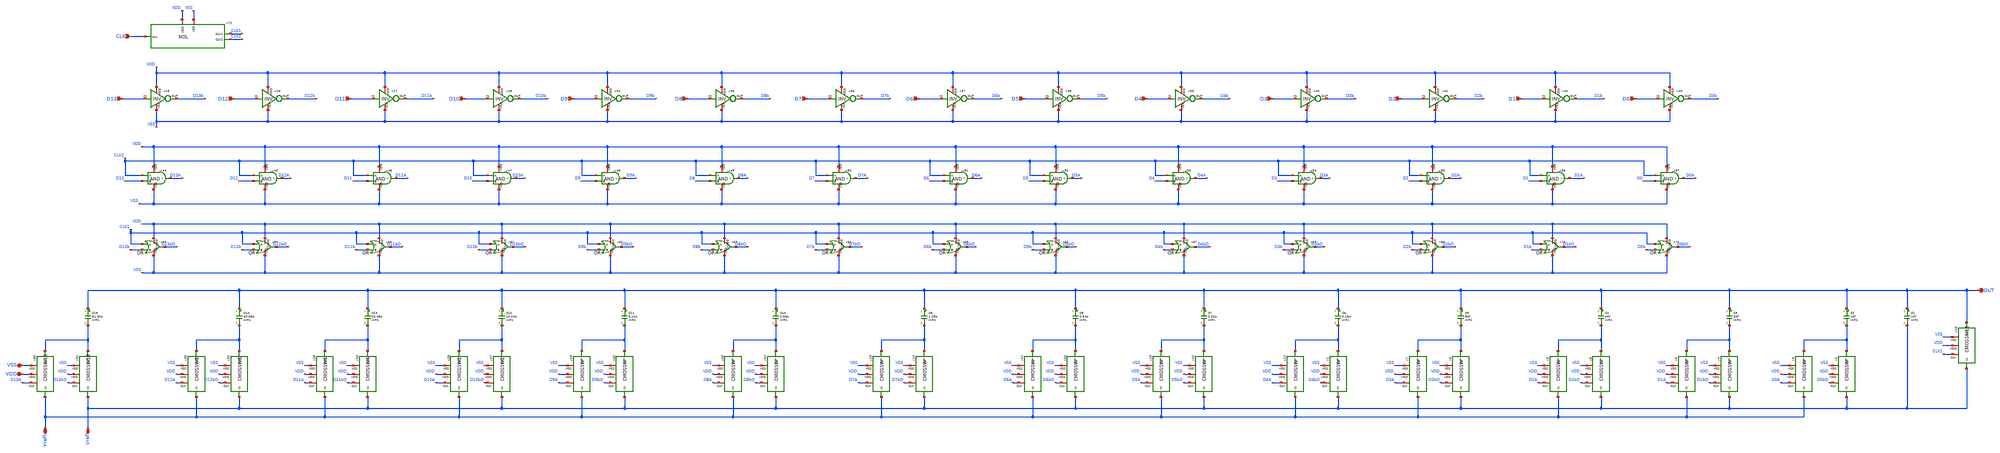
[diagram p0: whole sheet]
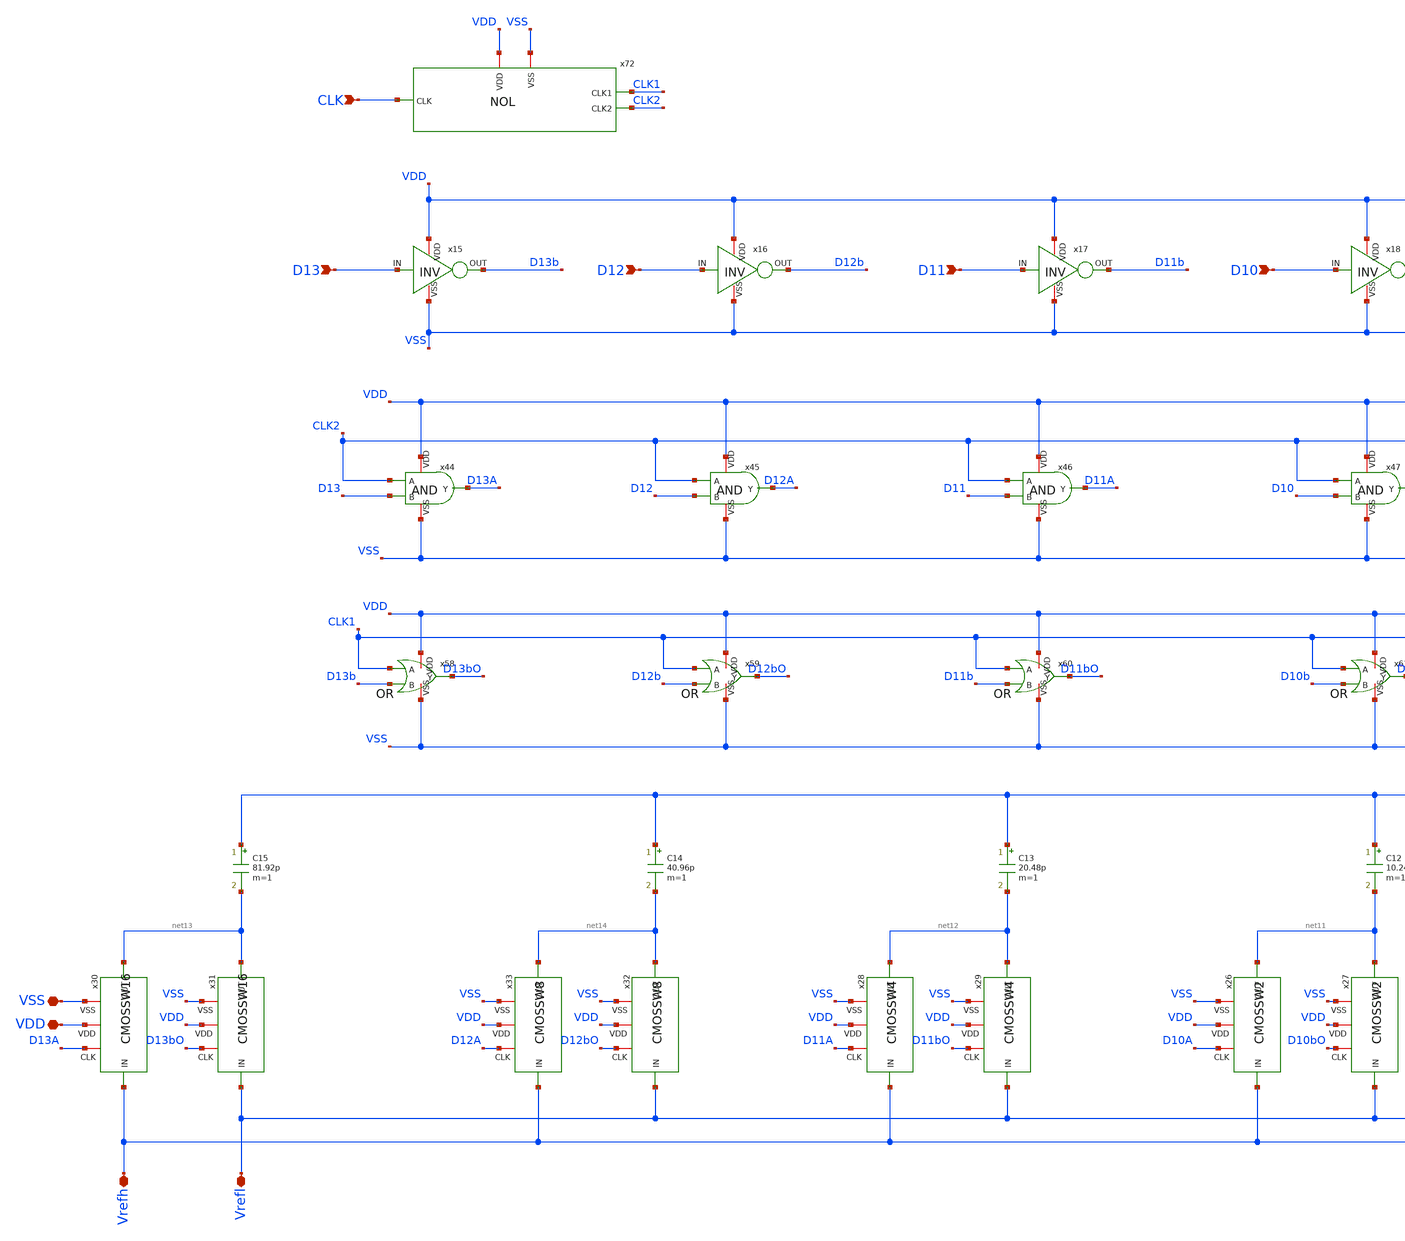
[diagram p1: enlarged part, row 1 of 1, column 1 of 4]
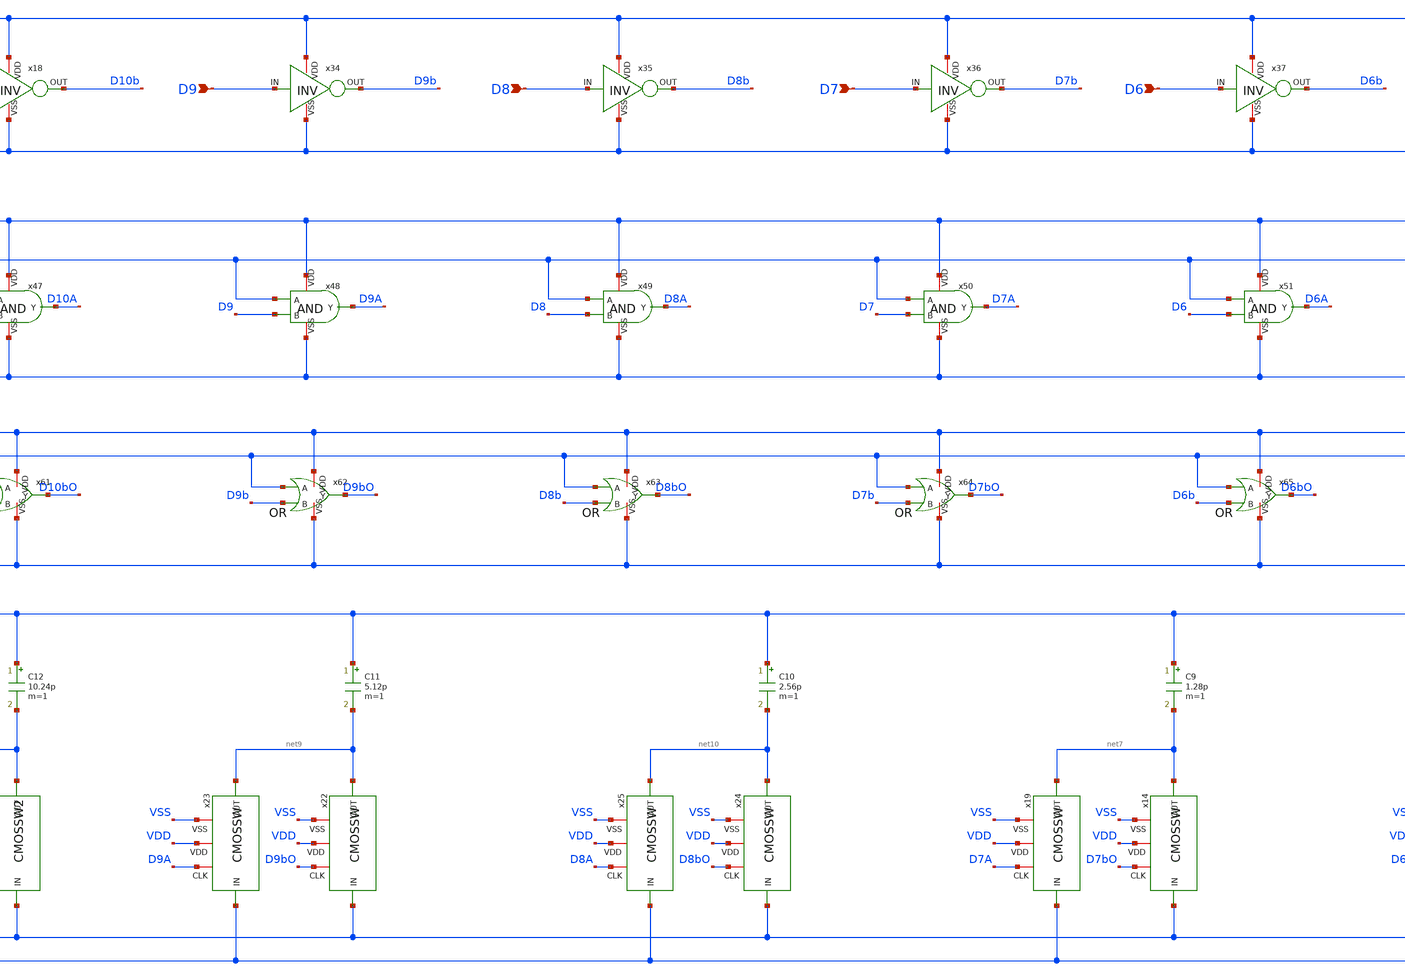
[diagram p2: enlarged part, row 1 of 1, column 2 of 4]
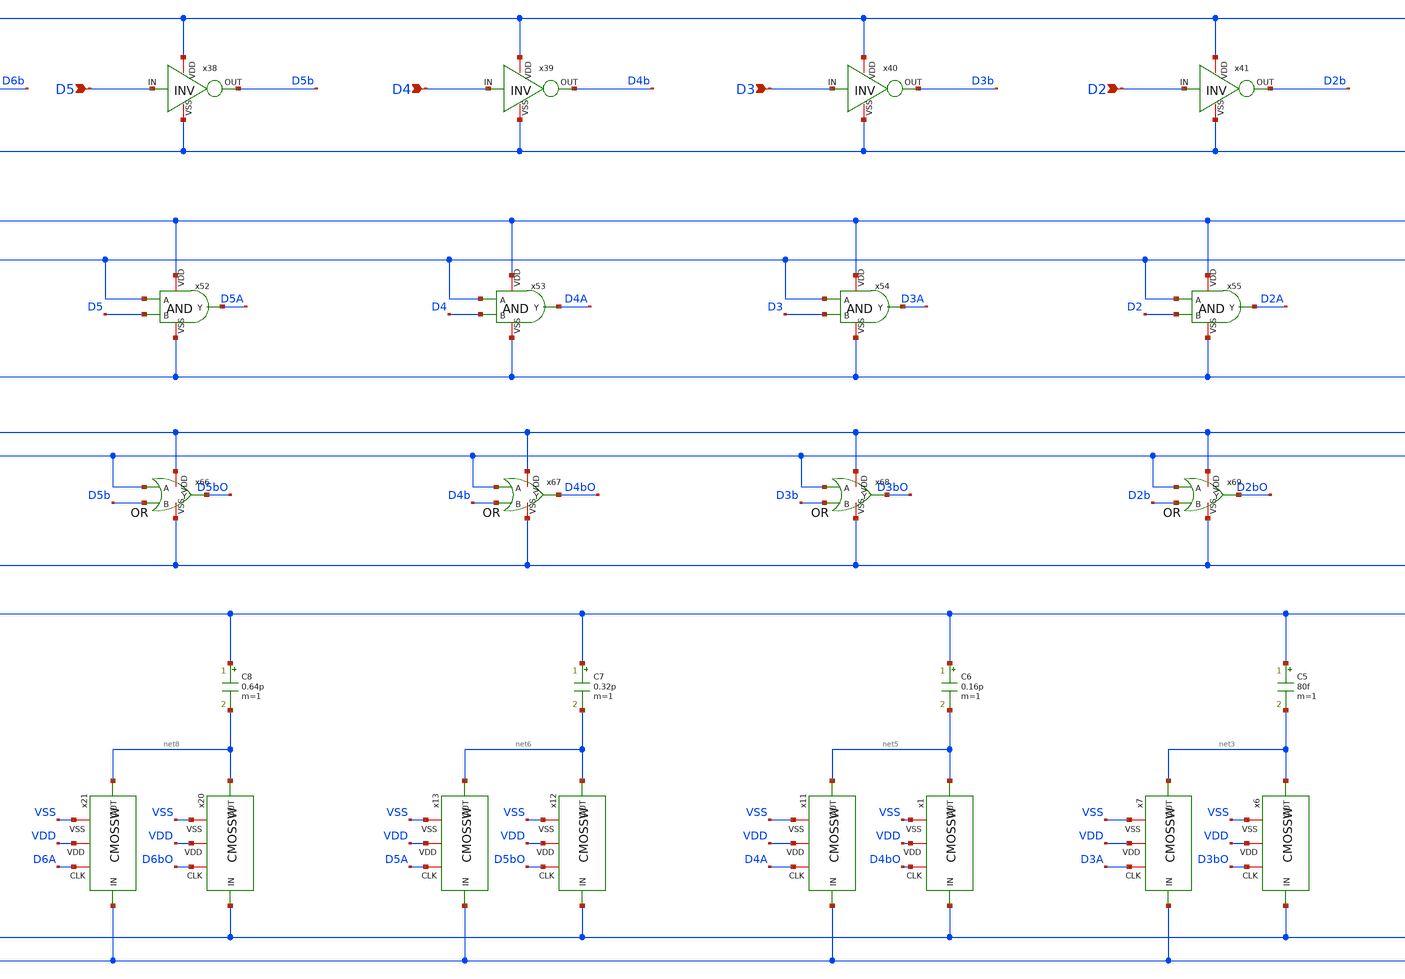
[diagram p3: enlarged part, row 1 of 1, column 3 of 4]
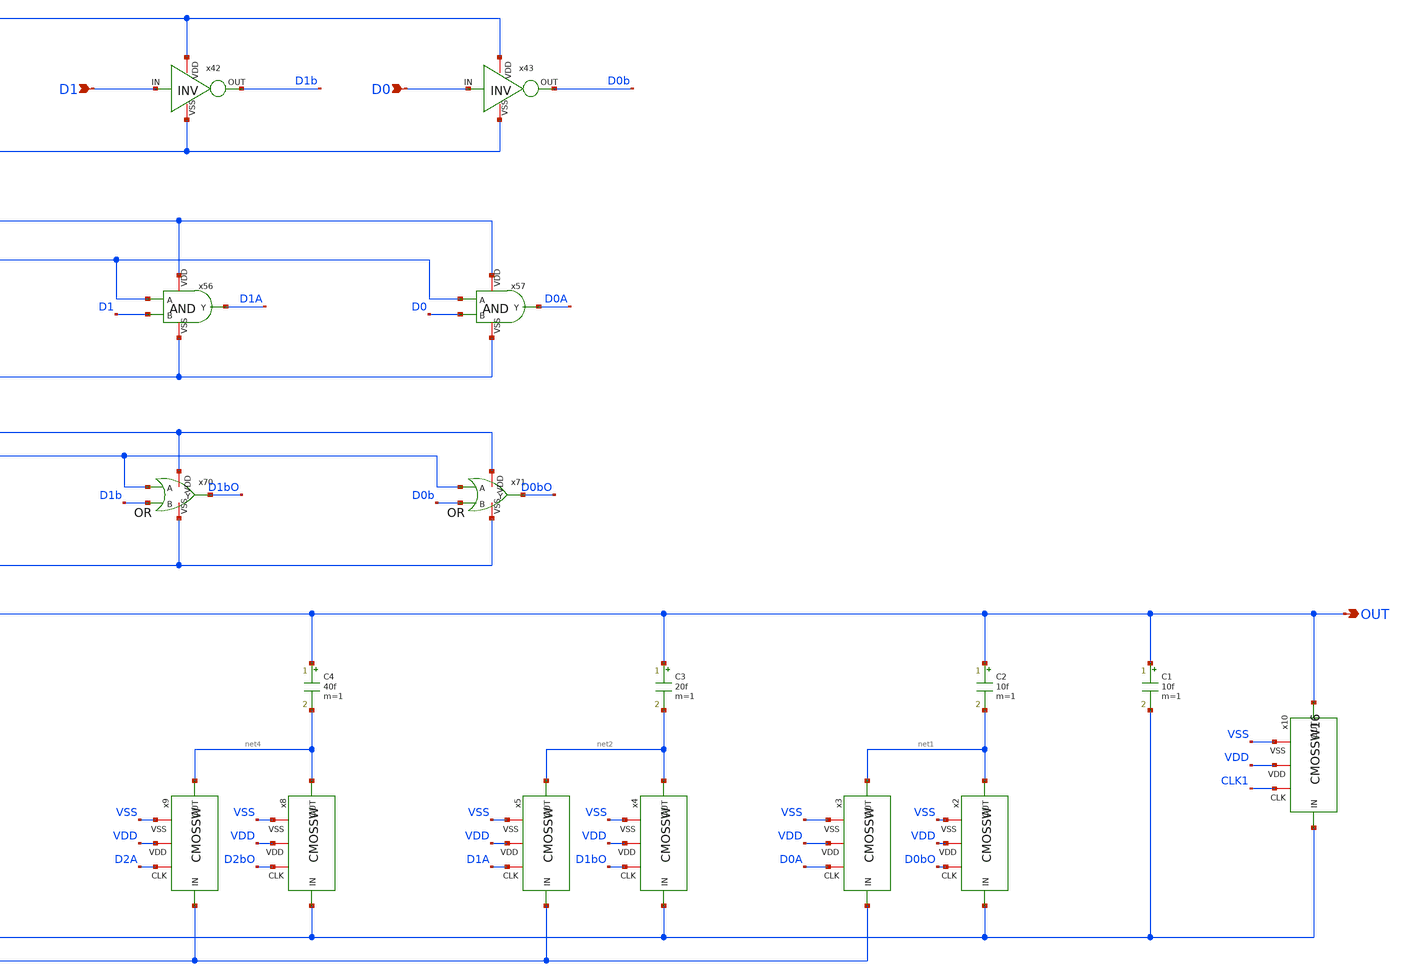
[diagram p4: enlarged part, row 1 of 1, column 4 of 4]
** sch_path: CDAC.sch
**.subckt CDAC OUT Vrefh Vrefl D13 D12 D11 D10 VSS VDD D9 D8 D7 D6 D5 D4 D3 D2 D1 D0 CLK
*.opin OUT
*.iopin Vrefh
*.iopin Vrefl
*.ipin D13
*.ipin D12
*.ipin D11
*.ipin D10
*.iopin VSS
*.iopin VDD
*.ipin D9
*.ipin D8
*.ipin D7
*.ipin D6
*.ipin D5
*.ipin D4
*.ipin D3
*.ipin D2
*.ipin D1
*.ipin D0
*.ipin CLK
C1 OUT Vrefl 10f m=1
C2 OUT net1 10f m=1
C3 OUT net2 20f m=1
C4 OUT net4 40f m=1
C5 OUT net3 80f m=1
x2 D0bO VSS net1 Vrefl VDD CMOSSW
x3 D0A VSS net1 Vrefh VDD CMOSSW
x4 D1bO VSS net2 Vrefl VDD CMOSSW
x5 D1A VSS net2 Vrefh VDD CMOSSW
x6 D3bO VSS net3 Vrefl VDD CMOSSW
x7 D3A VSS net3 Vrefh VDD CMOSSW
x8 D2bO VSS net4 Vrefl VDD CMOSSW
x9 D2A VSS net4 Vrefh VDD CMOSSW
x15 VDD D13b D13 VSS INV
x16 VDD D12b D12 VSS INV
x17 VDD D11b D11 VSS INV
x18 VDD D10b D10 VSS INV
C6 OUT net5 0.16p m=1
C7 OUT net6 0.32p m=1
C8 OUT net8 0.64p m=1
C9 OUT net7 1.28p m=1
x1 D4bO VSS net5 Vrefl VDD CMOSSW
x11 D4A VSS net5 Vrefh VDD CMOSSW
x12 D5bO VSS net6 Vrefl VDD CMOSSW
x13 D5A VSS net6 Vrefh VDD CMOSSW
x14 D7bO VSS net7 Vrefl VDD CMOSSW
x19 D7A VSS net7 Vrefh VDD CMOSSW
x20 D6bO VSS net8 Vrefl VDD CMOSSW
x21 D6A VSS net8 Vrefh VDD CMOSSW
C10 OUT net10 2.56p m=1
C11 OUT net9 5.12p m=1
x22 D9bO VSS net9 Vrefl VDD CMOSSW
x23 D9A VSS net9 Vrefh VDD CMOSSW
x24 D8bO VSS net10 Vrefl VDD CMOSSW
x25 D8A VSS net10 Vrefh VDD CMOSSW
C12 OUT net11 10.24p m=1
C13 OUT net12 20.48p m=1
C14 OUT net14 40.96p m=1
C15 OUT net13 81.92p m=1
x34 VDD D9b D9 VSS INV
x35 VDD D8b D8 VSS INV
x36 VDD D7b D7 VSS INV
x37 VDD D6b D6 VSS INV
x38 VDD D5b D5 VSS INV
x39 VDD D4b D4 VSS INV
x40 VDD D3b D3 VSS INV
x41 VDD D2b D2 VSS INV
x42 VDD D1b D1 VSS INV
x43 VDD D0b D0 VSS INV
x44 VDD D13A CLK2 D13 VSS AND
x45 VDD D12A CLK2 D12 VSS AND
x46 VDD D11A CLK2 D11 VSS AND
x47 VDD D10A CLK2 D10 VSS AND
x48 VDD D9A CLK2 D9 VSS AND
x49 VDD D8A CLK2 D8 VSS AND
x50 VDD D7A CLK2 D7 VSS AND
x51 VDD D6A CLK2 D6 VSS AND
x52 VDD D5A CLK2 D5 VSS AND
x53 VDD D4A CLK2 D4 VSS AND
x54 VDD D3A CLK2 D3 VSS AND
x55 VDD D2A CLK2 D2 VSS AND
x56 VDD D1A CLK2 D1 VSS AND
x57 VDD D0A CLK2 D0 VSS AND
x58 VDD CLK1 D13bO D13b VSS OR
x59 VDD CLK1 D12bO D12b VSS OR
x60 VDD CLK1 D11bO D11b VSS OR
x61 VDD CLK1 D10bO D10b VSS OR
x62 VDD CLK1 D9bO D9b VSS OR
x63 VDD CLK1 D8bO D8b VSS OR
x64 VDD CLK1 D7bO D7b VSS OR
x65 VDD CLK1 D6bO D6b VSS OR
x66 VDD CLK1 D5bO D5b VSS OR
x67 VDD CLK1 D4bO D4b VSS OR
x68 VDD CLK1 D3bO D3b VSS OR
x69 VDD CLK1 D2bO D2b VSS OR
x70 VDD CLK1 D1bO D1b VSS OR
x71 VDD CLK1 D0bO D0b VSS OR
x72 VDD CLK CLK1 VSS CLK2 NOL
x30 D13A VSS net13 Vrefh VDD CMOSSW16
x31 D13bO VSS net13 Vrefl VDD CMOSSW16
x33 D12A VSS net14 Vrefh VDD CMOSSW8
x32 D12bO VSS net14 Vrefl VDD CMOSSW8
x28 D11A VSS net12 Vrefh VDD CMOSSW4
x29 D11bO VSS net12 Vrefl VDD CMOSSW4
x26 D10A VSS net11 Vrefh VDD CMOSSW2
x27 D10bO VSS net11 Vrefl VDD CMOSSW2
x10 CLK1 VSS OUT Vrefl VDD CMOSSW16
**.ends

* expanding   symbol:  C:/Users/ISLab2/Documents/minimal_LR/CMOSSW.sym # of pins=5
** sym_path: CMOSSW.sym
** sch_path: CMOSSW.sch
.subckt CMOSSW CLK VSS OUT IN VDD
*.ipin IN
*.iopin VDD
*.iopin VSS
*.opin OUT
*.iopin CLK
M1 OUT CLK IN VSS nch w=10u l=0.35u as=0 ps=0 ad=0 pd=0 m=1
M2 OUT net1 IN VDD pch w=10u l=0.35u as=0 ps=0 ad=0 pd=0 m=1
**** begin user architecture code


.include C:/Users/ISLab2/Documents/minimal_LR/minimal.txt

**** end user architecture code
x1 VDD net1 CLK VSS INV
.ends


* expanding   symbol:  C:/Users/ISLab2/Documents/minimal_LR/INV.sym # of pins=4
** sym_path: INV.sym
** sch_path: INV.sch
.subckt INV VDD OUT IN VSS
*.opin OUT
*.ipin IN
*.iopin VDD
*.iopin VSS
M2 OUT IN VDD VDD pch w=10u l=0.35u as=0 ps=0 ad=0 pd=0 m=1
M1 OUT IN VSS VSS nch w=5u l=0.35u as=0 ps=0 ad=0 pd=0 m=1
.ends


* expanding   symbol:  C:/Users/ISLab2/Documents/minimal_LR/AND.sym # of pins=5
** sym_path: AND.sym
** sch_path: AND.sch
.subckt AND VDD Y A B VSS
*.iopin VDD
*.ipin A
*.ipin B
*.iopin VSS
*.opin Y
M1 net1 A net2 VSS nch w=3.5u l=0.35u as=0 ps=0 ad=0 pd=0 m=1
M2 net1 B VDD VDD pch w=3.5u l=0.35u as=0 ps=0 ad=0 pd=0 m=1
M3 net1 A VDD VDD pch w=3.5u l=0.35u as=0 ps=0 ad=0 pd=0 m=1
M4 net2 B VSS VSS nch w=3.5u l=0.35u as=0 ps=0 ad=0 pd=0 m=1
M5 Y net1 VDD VDD pch w=3.5u l=0.35u as=0 ps=0 ad=0 pd=0 m=1
M6 Y net1 VSS VSS nch w=3.5u l=0.35u as=0 ps=0 ad=0 pd=0 m=1
.ends


* expanding   symbol:  C:/Users/ISLab2/Documents/minimal_LR/OR.sym # of pins=5
** sym_path: OR.sym
** sch_path: OR.sch
.subckt OR VDD A Y B VSS
*.iopin VDD
*.ipin A
*.ipin B
*.iopin VSS
*.opin Y
M1 net1 A VSS VSS nch w=3.5u l=0.35u as=0 ps=0 ad=0 pd=0 m=1
M2 net2 A VDD VDD pch w=3.5u l=0.35u as=0 ps=0 ad=0 pd=0 m=1
M3 net1 B net2 VDD pch w=3.5u l=0.35u as=0 ps=0 ad=0 pd=0 m=1
M4 net1 B VSS VSS nch w=3.5u l=0.35u as=0 ps=0 ad=0 pd=0 m=1
M5 Y net1 VDD VDD pch w=3.5u l=0.35u as=0 ps=0 ad=0 pd=0 m=1
M6 Y net1 VSS VSS nch w=3.5u l=0.35u as=0 ps=0 ad=0 pd=0 m=1
.ends


* expanding   symbol:  C:/Users/ISLab2/Documents/minimal_LR/NOL.sym # of pins=5
** sym_path: NOL.sym
** sch_path: NOL.sch
.subckt NOL VDD CLK CLK1 VSS CLK2
*.ipin CLK
*.opin CLK1
*.opin CLK2
*.iopin VDD
*.iopin VSS
x3 VDD net1 CLK VSS INV
x1 VDD CLK net9 CLK2 VSS NOR
x2 VDD CLK1 net2 net1 VSS NOR
x4 VDD net3 net2 VSS INV
x5 VDD net4 net3 VSS INV
x6 VDD net5 net4 VSS INV
x7 VDD net17 net5 VSS INV
x8 VDD net6 net9 VSS INV
x9 VDD net7 net6 VSS INV
x10 VDD net8 net7 VSS INV
x11 VDD net13 net8 VSS INV
x12 VDD net10 net13 VSS INV
x13 VDD net11 net10 VSS INV
x14 VDD net12 net11 VSS INV
x15 VDD net32 net12 VSS INV
x16 VDD net14 net17 VSS INV
x17 VDD net15 net14 VSS INV
x18 VDD net16 net15 VSS INV
x19 VDD net33 net16 VSS INV
x20 VDD net18 net33 VSS INV
x21 VDD net19 net18 VSS INV
x22 VDD net20 net19 VSS INV
x23 VDD net24 net20 VSS INV
x24 VDD net21 net24 VSS INV
x25 VDD net22 net21 VSS INV
x26 VDD net23 net22 VSS INV
x27 VDD CLK2 net23 VSS INV
x28 VDD net25 net32 VSS INV
x29 VDD net26 net25 VSS INV
x30 VDD net27 net26 VSS INV
x31 VDD net31 net27 VSS INV
x32 VDD net28 net31 VSS INV
x33 VDD net29 net28 VSS INV
x34 VDD net30 net29 VSS INV
x35 VDD CLK1 net30 VSS INV
.ends


* expanding   symbol:  C:/Users/ISLab2/Documents/minimal_LR/CMOSSW16.sym # of pins=5
** sym_path: CMOSSW16.sym
** sch_path: CMOSSW16.sch
.subckt CMOSSW16 CLK VSS OUT IN VDD
*.ipin IN
*.opin OUT
*.iopin VSS
*.iopin VDD
*.iopin CLK
x1 CLK VSS OUT IN VDD CMOSSW8
x2 CLK VSS OUT IN VDD CMOSSW8
.ends


* expanding   symbol:  C:/Users/ISLab2/Documents/minimal_LR/CMOSSW8.sym # of pins=5
** sym_path: CMOSSW8.sym
** sch_path: CMOSSW8.sch
.subckt CMOSSW8 CLK VSS OUT IN VDD
*.ipin IN
*.opin OUT
*.iopin VSS
*.iopin VDD
*.iopin CLK
x1 CLK VSS OUT IN VDD CMOSSW4
x2 CLK VSS OUT IN VDD CMOSSW4
.ends


* expanding   symbol:  C:/Users/ISLab2/Documents/minimal_LR/CMOSSW4.sym # of pins=5
** sym_path: CMOSSW4.sym
** sch_path: CMOSSW4.sch
.subckt CMOSSW4 CLK VSS OUT IN VDD
*.ipin IN
*.opin OUT
*.iopin VSS
*.iopin VDD
*.iopin CLK
x1 CLK VSS OUT IN VDD CMOSSW2
x2 CLK VSS OUT IN VDD CMOSSW2
.ends


* expanding   symbol:  C:/Users/ISLab2/Documents/minimal_LR/CMOSSW2.sym # of pins=5
** sym_path: CMOSSW2.sym
** sch_path: CMOSSW2.sch
.subckt CMOSSW2 CLK VSS OUT IN VDD
*.ipin IN
*.opin OUT
*.iopin VSS
*.iopin VDD
*.iopin CLK
x1 CLK VSS OUT IN VDD CMOSSW
x2 CLK VSS OUT IN VDD CMOSSW
.ends


* expanding   symbol:  C:/Users/ISLab2/Documents/minimal_LR/NOR.sym # of pins=5
** sym_path: NOR.sym
** sch_path: NOR.sch
.subckt NOR VDD A Y B VSS
*.iopin VDD
*.ipin A
*.ipin B
*.iopin VSS
*.opin Y
M1 Y A VSS VSS nch w=3.5u l=0.35u as=0 ps=0 ad=0 pd=0 m=1
M2 net1 A VDD VDD pch w=3.5u l=0.35u as=0 ps=0 ad=0 pd=0 m=1
M3 Y B net1 VDD pch w=3.5u l=0.35u as=0 ps=0 ad=0 pd=0 m=1
M4 Y B VSS VSS nch w=3.5u l=0.35u as=0 ps=0 ad=0 pd=0 m=1
**** begin user architecture code


.include C:/Users/ISLab2/Documents/minimal_LR/minimal.txt

**** end user architecture code
.ends

.end
